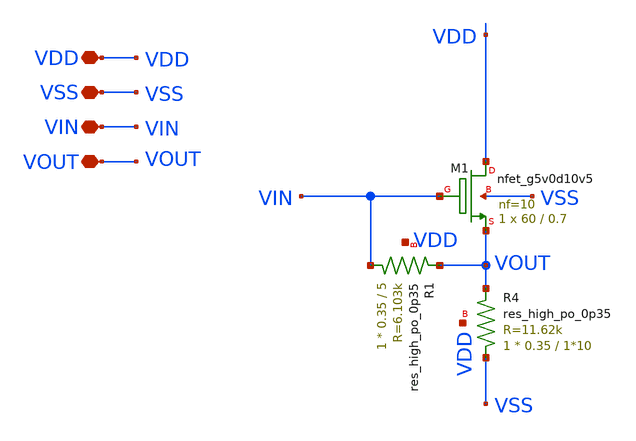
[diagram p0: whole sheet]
** sch_path: amplifiers/single_stage_amps/stange_stages/source_follower_1/source_follower_1_stage.sch
**.subckt source_follower_1_stage VDD VSS VIN VOUT
*.iopin VDD
*.iopin VSS
*.iopin VIN
*.iopin VOUT
XM1 VDD VIN VOUT VSS sky130_fd_pr__nfet_g5v0d10v5 L=0.7 W=60 nf=10 ad='int((nf+1)/2) * W/nf * 0.29' as='int((nf+2)/2) * W/nf * 0.29'
+ pd='2*int((nf+1)/2) * (W/nf + 0.29)' ps='2*int((nf+2)/2) * (W/nf + 0.29)' nrd='0.29 / W' nrs='0.29 / W'
+ sa=0 sb=0 sd=0 mult=1 m=1
XR1 VIN VOUT VDD sky130_fd_pr__res_high_po_0p35 L=5 mult=1 m=1
XR4 VSS VOUT VDD sky130_fd_pr__res_high_po_0p35 L=1*10 mult=1 m=1
**.ends
.end
